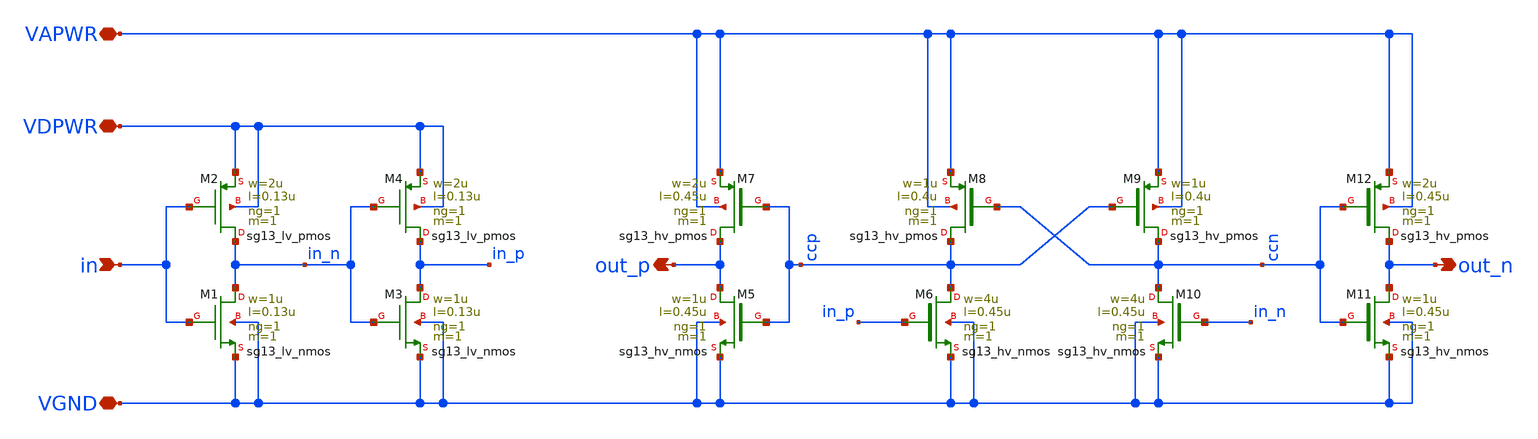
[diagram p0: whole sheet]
** sch_path: ihp-sg13cmos5l/libs.tech/xschem/hm_analog/lv2hv.sch
**.subckt lv2hv VAPWR VGND in VDPWR out_p out_n
*.iopin VAPWR
*.iopin VGND
*.ipin in
*.iopin VDPWR
*.opin out_p
*.opin out_n
XM1 in_n in VGND VGND sg13_lv_nmos w=1u l=0.13u ng=1 m=1 mm_ok=1
XM2 in_n in VDPWR VDPWR sg13_lv_pmos w=2u l=0.13u ng=1 m=1 mm_ok=1
XM3 in_p in_n VGND VGND sg13_lv_nmos w=1u l=0.13u ng=1 m=1 mm_ok=1
XM4 in_p in_n VDPWR VDPWR sg13_lv_pmos w=2u l=0.13u ng=1 m=1 mm_ok=1
XM5 out_p ccp VGND VGND sg13_hv_nmos w=1u l=0.45u ng=1 m=1 mm_ok=1
XM6 ccp in_p VGND VGND sg13_hv_nmos w=4u l=0.45u ng=1 m=1 mm_ok=1
XM7 out_p ccp VAPWR VAPWR sg13_hv_pmos w=2u l=0.45u ng=1 m=1 mm_ok=1
XM8 ccp ccn VAPWR VAPWR sg13_hv_pmos w=1u l=0.4u ng=1 m=1 mm_ok=1
XM9 ccn ccp VAPWR VAPWR sg13_hv_pmos w=1u l=0.4u ng=1 m=1 mm_ok=1
XM10 ccn in_n VGND VGND sg13_hv_nmos w=4u l=0.45u ng=1 m=1 mm_ok=1
XM11 out_n ccn VGND VGND sg13_hv_nmos w=1u l=0.45u ng=1 m=1 mm_ok=1
XM12 out_n ccn VAPWR VAPWR sg13_hv_pmos w=2u l=0.45u ng=1 m=1 mm_ok=1
**.ends
.end
